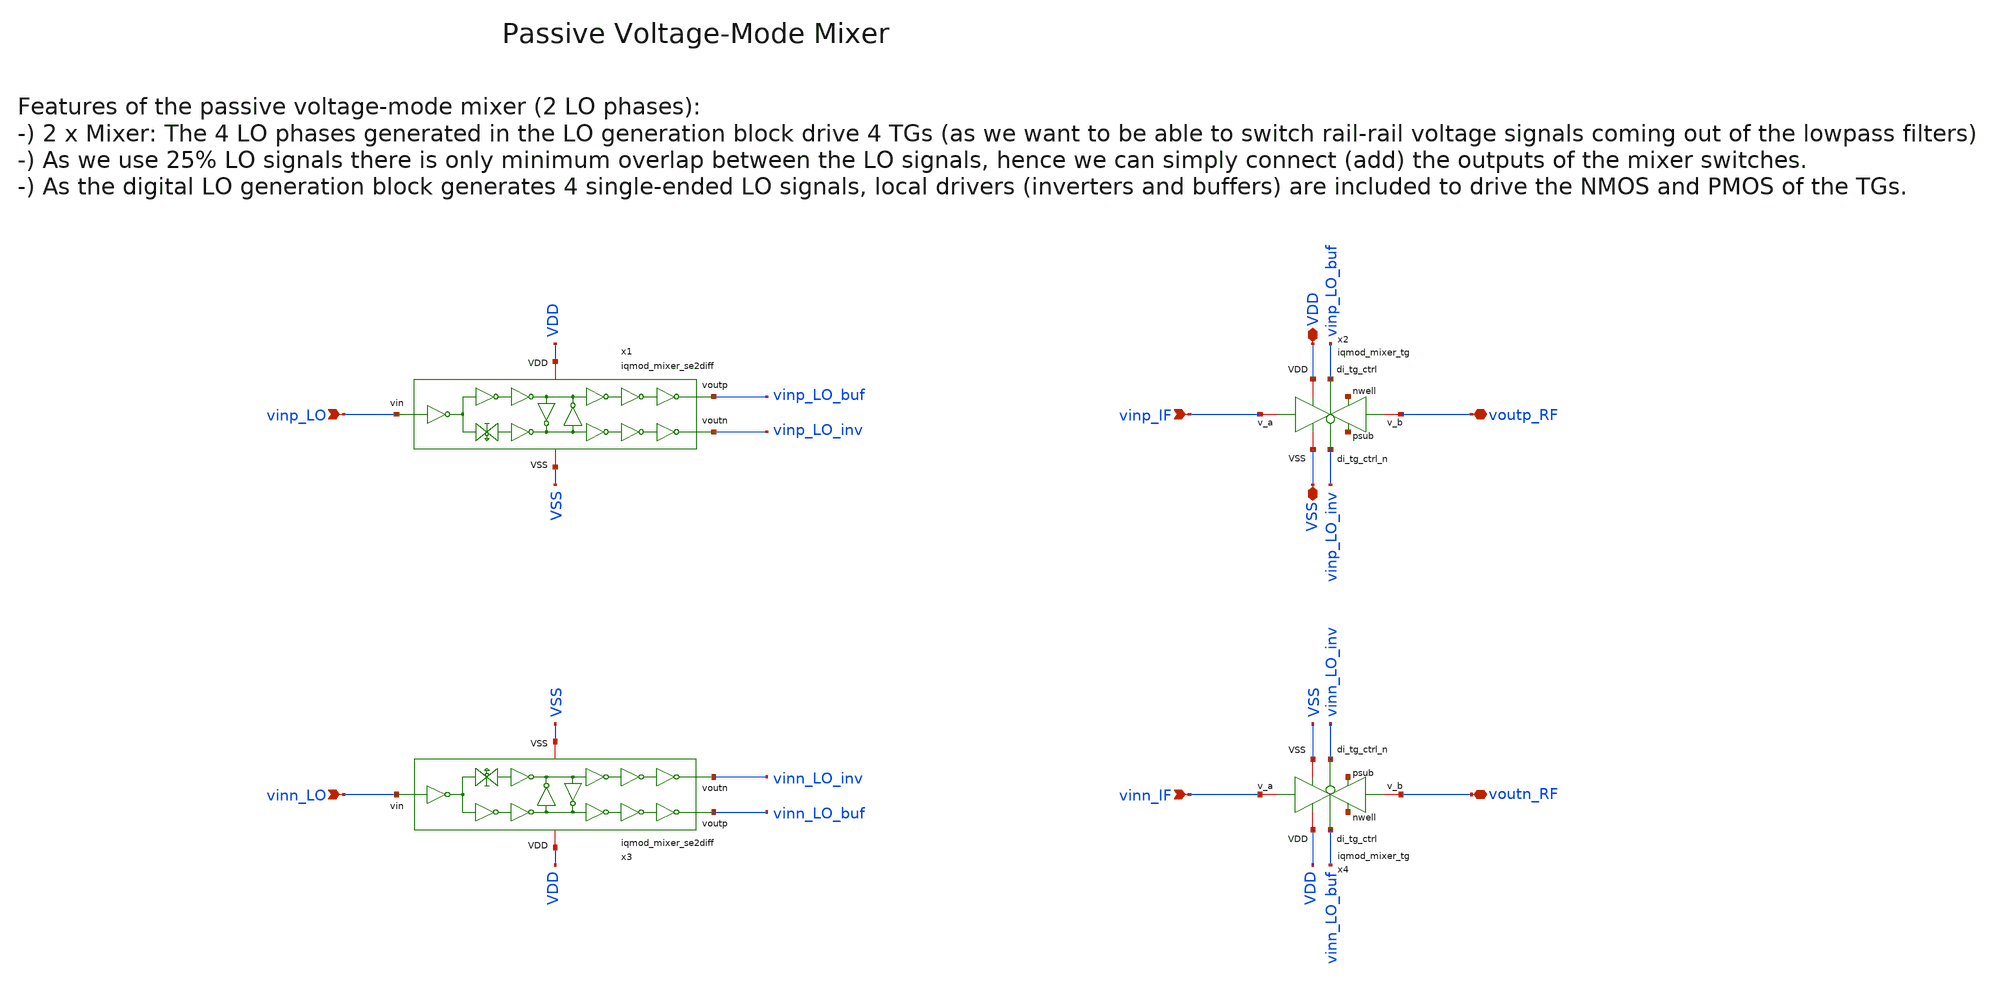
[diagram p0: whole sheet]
** sch_path: ihp130/macros/iqmod/schematic/xschem/iqmod_mixer.sch
**.subckt iqmod_mixer VDD VSS vinp_IF vinn_IF voutp_RF vinp_LO vinn_LO voutn_RF
*.iopin VDD
*.iopin VSS
*.ipin vinp_IF
*.ipin vinn_IF
*.iopin voutp_RF
*.ipin vinp_LO
*.ipin vinn_LO
*.iopin voutn_RF
x2 net1 net2 VDD vinp_LO_buf VSS voutp_RF vinp_IF vinp_LO_inv iqmod_mixer_tg
x4 net3 net4 VDD vinn_LO_buf VSS voutn_RF vinn_IF vinn_LO_inv iqmod_mixer_tg
x1 VDD vinp_LO vinp_LO_buf VSS vinp_LO_inv iqmod_mixer_se2diff
x3 VDD vinn_LO vinn_LO_buf VSS vinn_LO_inv iqmod_mixer_se2diff
**.ends
.end
